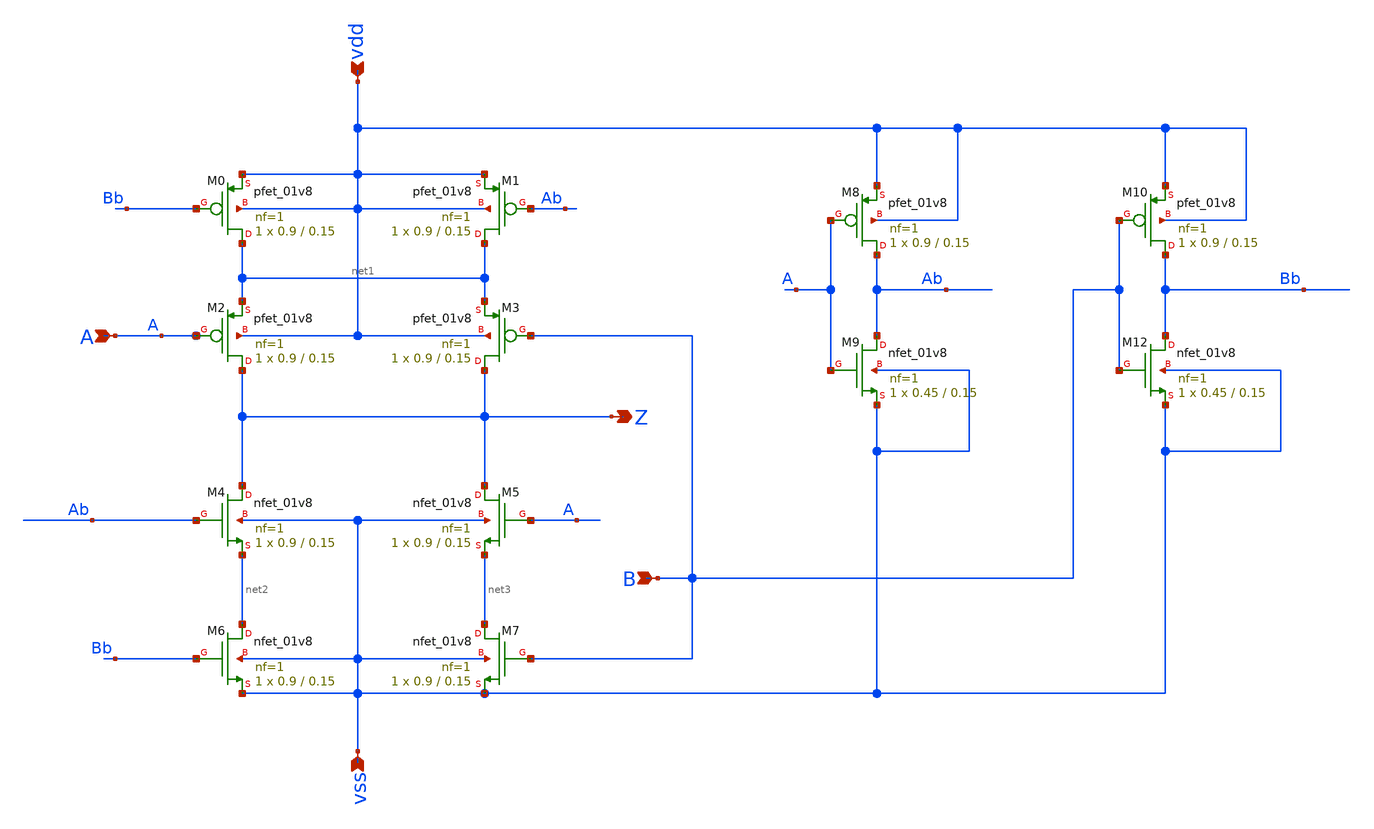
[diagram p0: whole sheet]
** sch_path: track_vlsi/lado/sch/xor.sch
**.subckt xor A vss vdd Z B
*.ipin A
*.ipin vss
*.ipin vdd
*.opin Z
*.ipin B
XM0 net1 Bb vdd vdd sky130_fd_pr__pfet_01v8 L=0.15 W=0.9 nf=1 ad='int((nf+1)/2) * W/nf * 0.29' as='int((nf+2)/2) * W/nf * 0.29'
+ pd='2*int((nf+1)/2) * (W/nf + 0.29)' ps='2*int((nf+2)/2) * (W/nf + 0.29)' nrd='0.29 / W' nrs='0.29 / W'
+ sa=0 sb=0 sd=0 mult=1 m=1
XM5 Z A net3 vss sky130_fd_pr__nfet_01v8 L=0.15 W=0.9 nf=1 ad='int((nf+1)/2) * W/nf * 0.29' as='int((nf+2)/2) * W/nf * 0.29'
+ pd='2*int((nf+1)/2) * (W/nf + 0.29)' ps='2*int((nf+2)/2) * (W/nf + 0.29)' nrd='0.29 / W' nrs='0.29 / W'
+ sa=0 sb=0 sd=0 mult=1 m=1
XM1 net1 Ab vdd vdd sky130_fd_pr__pfet_01v8 L=0.15 W=0.9 nf=1 ad='int((nf+1)/2) * W/nf * 0.29' as='int((nf+2)/2) * W/nf * 0.29'
+ pd='2*int((nf+1)/2) * (W/nf + 0.29)' ps='2*int((nf+2)/2) * (W/nf + 0.29)' nrd='0.29 / W' nrs='0.29 / W'
+ sa=0 sb=0 sd=0 mult=1 m=1
XM2 Z A net1 vdd sky130_fd_pr__pfet_01v8 L=0.15 W=0.9 nf=1 ad='int((nf+1)/2) * W/nf * 0.29' as='int((nf+2)/2) * W/nf * 0.29'
+ pd='2*int((nf+1)/2) * (W/nf + 0.29)' ps='2*int((nf+2)/2) * (W/nf + 0.29)' nrd='0.29 / W' nrs='0.29 / W'
+ sa=0 sb=0 sd=0 mult=1 m=1
XM4 Z Ab net2 vss sky130_fd_pr__nfet_01v8 L=0.15 W=0.9 nf=1 ad='int((nf+1)/2) * W/nf * 0.29' as='int((nf+2)/2) * W/nf * 0.29'
+ pd='2*int((nf+1)/2) * (W/nf + 0.29)' ps='2*int((nf+2)/2) * (W/nf + 0.29)' nrd='0.29 / W' nrs='0.29 / W'
+ sa=0 sb=0 sd=0 mult=1 m=1
XM6 net2 Bb vss vss sky130_fd_pr__nfet_01v8 L=0.15 W=0.9 nf=1 ad='int((nf+1)/2) * W/nf * 0.29' as='int((nf+2)/2) * W/nf * 0.29'
+ pd='2*int((nf+1)/2) * (W/nf + 0.29)' ps='2*int((nf+2)/2) * (W/nf + 0.29)' nrd='0.29 / W' nrs='0.29 / W'
+ sa=0 sb=0 sd=0 mult=1 m=1
XM8 Ab A vdd vdd sky130_fd_pr__pfet_01v8 L=0.15 W=0.9 nf=1 ad='int((nf+1)/2) * W/nf * 0.29' as='int((nf+2)/2) * W/nf * 0.29'
+ pd='2*int((nf+1)/2) * (W/nf + 0.29)' ps='2*int((nf+2)/2) * (W/nf + 0.29)' nrd='0.29 / W' nrs='0.29 / W'
+ sa=0 sb=0 sd=0 mult=1 m=1
XM9 Ab A vss vss sky130_fd_pr__nfet_01v8 L=0.15 W=0.45 nf=1 ad='int((nf+1)/2) * W/nf * 0.29' as='int((nf+2)/2) * W/nf * 0.29'
+ pd='2*int((nf+1)/2) * (W/nf + 0.29)' ps='2*int((nf+2)/2) * (W/nf + 0.29)' nrd='0.29 / W' nrs='0.29 / W'
+ sa=0 sb=0 sd=0 mult=1 m=1
XM3 Z B net1 vdd sky130_fd_pr__pfet_01v8 L=0.15 W=0.9 nf=1 ad='int((nf+1)/2) * W/nf * 0.29' as='int((nf+2)/2) * W/nf * 0.29'
+ pd='2*int((nf+1)/2) * (W/nf + 0.29)' ps='2*int((nf+2)/2) * (W/nf + 0.29)' nrd='0.29 / W' nrs='0.29 / W'
+ sa=0 sb=0 sd=0 mult=1 m=1
XM12 Bb B vss vss sky130_fd_pr__nfet_01v8 L=0.15 W=0.45 nf=1 ad='int((nf+1)/2) * W/nf * 0.29' as='int((nf+2)/2) * W/nf * 0.29'
+ pd='2*int((nf+1)/2) * (W/nf + 0.29)' ps='2*int((nf+2)/2) * (W/nf + 0.29)' nrd='0.29 / W' nrs='0.29 / W'
+ sa=0 sb=0 sd=0 mult=1 m=1
XM7 net3 B vss vss sky130_fd_pr__nfet_01v8 L=0.15 W=0.9 nf=1 ad='int((nf+1)/2) * W/nf * 0.29' as='int((nf+2)/2) * W/nf * 0.29'
+ pd='2*int((nf+1)/2) * (W/nf + 0.29)' ps='2*int((nf+2)/2) * (W/nf + 0.29)' nrd='0.29 / W' nrs='0.29 / W'
+ sa=0 sb=0 sd=0 mult=1 m=1
XM10 Bb B vdd vdd sky130_fd_pr__pfet_01v8 L=0.15 W=0.9 nf=1 ad='int((nf+1)/2) * W/nf * 0.29' as='int((nf+2)/2) * W/nf * 0.29'
+ pd='2*int((nf+1)/2) * (W/nf + 0.29)' ps='2*int((nf+2)/2) * (W/nf + 0.29)' nrd='0.29 / W' nrs='0.29 / W'
+ sa=0 sb=0 sd=0 mult=1 m=1
**.ends
.end
